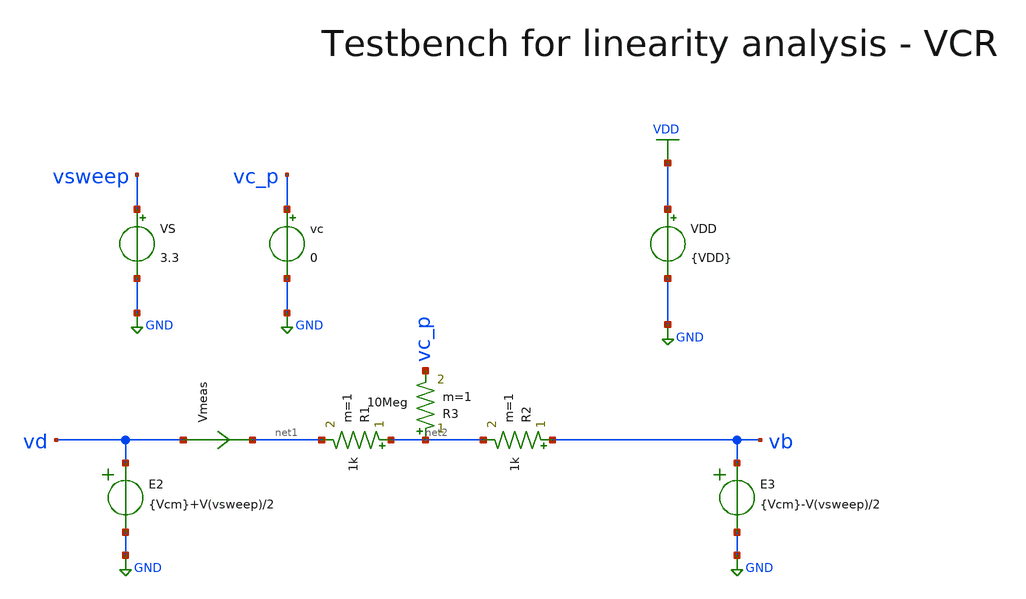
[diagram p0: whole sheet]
** sch_path: macros/heichips26_analog_project/macros/yadav/testbenches/xschem/res_tb_linearity.sch
**.subckt res_tb_linearity
VDD VDD GND {VDD}
R1 net2 net1 1k m=1
VS vsweep GND 3.3
Vmeas vd net1 0
.save i(vmeas)
E2 vd GND VOL=' {Vcm}+V(vsweep)/2 '
E3 vb GND VOL=' {Vcm}-V(vsweep)/2 '
vc vc_p GND 0
R2 vb net2 1k m=1
R3 net2 vc_p 10Meg m=1
**** begin user architecture code

.lib cornerMOSlv.lib mos_tt
.lib cornerMOShv.lib mos_tt
.lib cornerRES.lib res_typ
.lib cornerDIO.lib dio_tt



* .include ../../../netlist/pex/inverter_magic_pex_3.spice
.param VDD=1.5
.csparam VDD=VDD
.param Vcm=VDD/2
.csparam Vcm=Vcm
.param temp=27
.options savecurrents klu method=gear reltol=1e-3 abstol=1e-15 gmin=1e-15
.control
let vcc = 0.0

save all
set appendwrite



repeat 5
  alter vc $&vcc

  * DC Sweep
  dc VS -1.5 1.5 1m
  remzerovec
  let vcc = vcc + 0.3
end
write @schname\.raw
set appendwrite

* Plotting
plot dc1.v(vsweep)/(dc1.i(Vmeas)) dc2.v(vsweep)/(dc2.i(Vmeas)) dc3.v(vsweep)/(dc3.i(Vmeas))
+ dc4.v(vsweep)/(dc4.i(Vmeas)) dc5.v(vsweep)/(dc5.i(Vmeas))


* Write Data
unset appendwrite
set wr_vecnames
set wr_singlescale
wrdata ../plot_simulations/data/@schname\.txt v(vc_p) dc1.v(vsweep)/(dc1.i(Vmeas))
+ dc2.v(vsweep)/(dc2.i(Vmeas)) dc3.v(vsweep)/(dc3.i(Vmeas)) dc4.v(vsweep)/(dc4.i(Vmeas)) dc5.v(vsweep)/(dc5.i(Vmeas))



*quit
.endc


**** end user architecture code
**.ends
.GLOBAL GND
.GLOBAL VDD
.end
